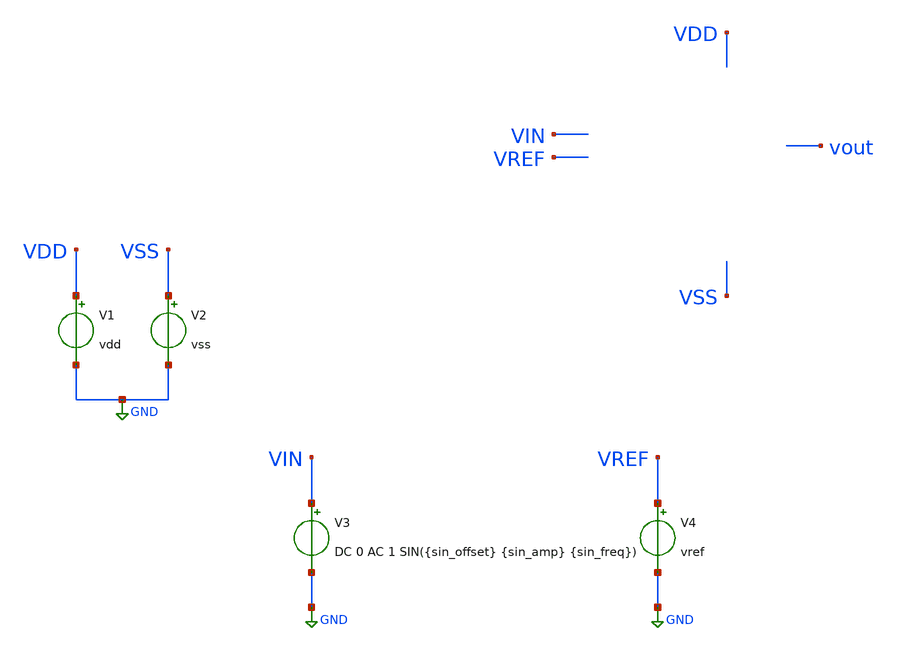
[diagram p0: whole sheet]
** sch_path: simulation/tb_comp_top.sch
**.subckt tb_comp_top
V1 VDD GND vdd
V2 VSS GND vss
V3 VIN GND DC 0 AC 1 SIN({sin_offset} {sin_amp} {sin_freq})
V4 VREF GND vref
**** begin user architecture code



# Model files
.lib /usr/local/share/pdk/sky130A/libs.tech/ngspice/sky130.lib.spice tt

# Main parameters
.param vdd=1.8 vss=0 vref='vdd/2' vhigh=1.8 vlow=0
.param sin_offset='vdd/2'
.param sin_amp='vdd/2'
.param sin_freq=10Meg
.param sin_period='1/sin_freq'
.param tran_step='sin_period/10'
.param tran_stop_time='sin_period*2'

# Component parameters



# Save settings
.save all


# Analysis
.op
.tran {tran_step} {tran_stop_time}

# Start control block
.control

# Run sim
run

# Expressions

# Save expressions

# Write to raw file
write tb_comp_top.raw
# wrdata custom_output.txt



.endc



**** end user architecture code
**.ends
.GLOBAL GND
.end
